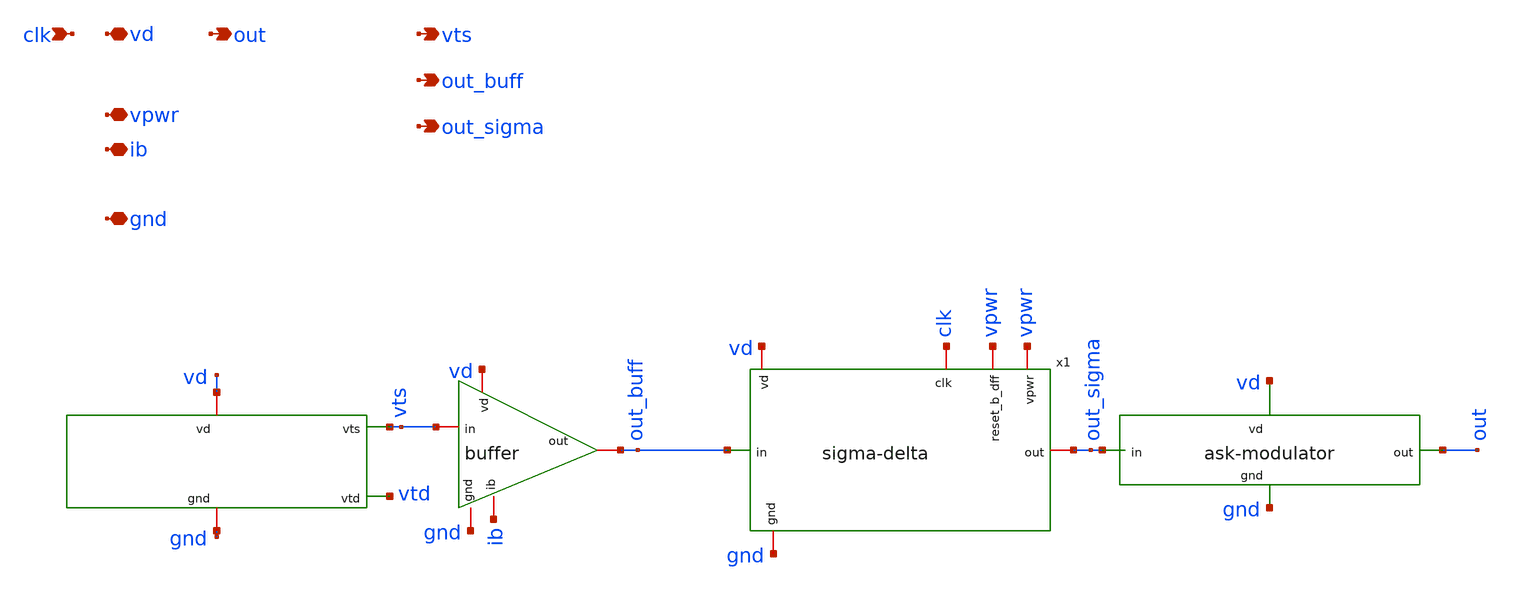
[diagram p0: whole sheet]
** sch_path: device-complete/xschem/device-complete.sch
* buffer/xschem/buffer.sch:
* Copyright 2020 Stefan Frederik Schippers
* Licensed under the Apache License, Version 2.0 (the "License");
**.subckt device-complete vd clk out vpwr ib gnd vts out_buff out_sigma
*.iopin vd
*.ipin clk
*.opin out
*.iopin vpwr
*.iopin ib
*.iopin gnd
*.opin vts
*.opin out_buff
*.opin out_sigma
x3 vd vts vtd gnd sensor
X2 vd vts out_buff ib gnd buffer
x4 vd out out_sigma gnd ask-modulator
x1 vpwr clk out_sigma out_buff vpwr gnd vd sigma-delta
**.ends

* expanding   symbol:  /foss/designs/temp-sensor/sensor/xschem/sensor.sym # of pins=4
** sym_path: sensor/xschem/sensor.sym
** sch_path: sensor/xschem/sensor.sch
.subckt sensor vd vts vtd gnd
*.iopin vd
*.opin vts
*.opin vtd
*.iopin gnd
XP1 a a vd vd sky130_fd_pr__pfet_01v8 L=1 W=4 nf=1 ad='int((nf+1)/2) * W/nf * 0.29' as='int((nf+2)/2) * W/nf * 0.29'
+ pd='2*int((nf+1)/2) * (W/nf + 0.29)' ps='2*int((nf+2)/2) * (W/nf + 0.29)' nrd='0.29 / W' nrs='0.29 / W'
+ sa=0 sb=0 sd=0 mult=1 m=1
XP2 c a d d sky130_fd_pr__pfet_01v8 L=1 W=8 nf=1 ad='int((nf+1)/2) * W/nf * 0.29' as='int((nf+2)/2) * W/nf * 0.29'
+ pd='2*int((nf+1)/2) * (W/nf + 0.29)' ps='2*int((nf+2)/2) * (W/nf + 0.29)' nrd='0.29 / W' nrs='0.29 / W'
+ sa=0 sb=0 sd=0 mult=1 m=1
XP3 d vtd vd vd sky130_fd_pr__pfet_01v8 L=1 W=2 nf=1 ad='int((nf+1)/2) * W/nf * 0.29' as='int((nf+2)/2) * W/nf * 0.29'
+ pd='2*int((nf+1)/2) * (W/nf + 0.29)' ps='2*int((nf+2)/2) * (W/nf + 0.29)' nrd='0.29 / W' nrs='0.29 / W'
+ sa=0 sb=0 sd=0 mult=1 m=1
XP4 vts vtd vd vd sky130_fd_pr__pfet_01v8 L=5 W=2 nf=1 ad='int((nf+1)/2) * W/nf * 0.29' as='int((nf+2)/2) * W/nf * 0.29'
+ pd='2*int((nf+1)/2) * (W/nf + 0.29)' ps='2*int((nf+2)/2) * (W/nf + 0.29)' nrd='0.29 / W' nrs='0.29 / W'
+ sa=0 sb=0 sd=0 mult=1 m=1
XP5 b vtd c c sky130_fd_pr__pfet_01v8 L=1 W=8 nf=1 ad='int((nf+1)/2) * W/nf * 0.29' as='int((nf+2)/2) * W/nf * 0.29'
+ pd='2*int((nf+1)/2) * (W/nf + 0.29)' ps='2*int((nf+2)/2) * (W/nf + 0.29)' nrd='0.29 / W' nrs='0.29 / W'
+ sa=0 sb=0 sd=0 mult=1 m=1
XP6 vtd vtd vts vts sky130_fd_pr__pfet_01v8 L=1 W=16 nf=1 ad='int((nf+1)/2) * W/nf * 0.29' as='int((nf+2)/2) * W/nf * 0.29'
+ pd='2*int((nf+1)/2) * (W/nf + 0.29)' ps='2*int((nf+2)/2) * (W/nf + 0.29)' nrd='0.29 / W' nrs='0.29 / W'
+ sa=0 sb=0 sd=0 mult=1 m=1
XN1 a b gnd gnd sky130_fd_pr__nfet_01v8 L=1 W=1 nf=1 ad='int((nf+1)/2) * W/nf * 0.29' as='int((nf+2)/2) * W/nf * 0.29'
+ pd='2*int((nf+1)/2) * (W/nf + 0.29)' ps='2*int((nf+2)/2) * (W/nf + 0.29)' nrd='0.29 / W' nrs='0.29 / W'
+ sa=0 sb=0 sd=0 mult=8 m=8
XN2 b b gnd gnd sky130_fd_pr__nfet_01v8 L=1 W=1 nf=1 ad='int((nf+1)/2) * W/nf * 0.29' as='int((nf+2)/2) * W/nf * 0.29'
+ pd='2*int((nf+1)/2) * (W/nf + 0.29)' ps='2*int((nf+2)/2) * (W/nf + 0.29)' nrd='0.29 / W' nrs='0.29 / W'
+ sa=0 sb=0 sd=0 mult=8 m=8
XN3 vtd b gnd gnd sky130_fd_pr__nfet_01v8 L=1 W=1 nf=1 ad='int((nf+1)/2) * W/nf * 0.29' as='int((nf+2)/2) * W/nf * 0.29'
+ pd='2*int((nf+1)/2) * (W/nf + 0.29)' ps='2*int((nf+2)/2) * (W/nf + 0.29)' nrd='0.29 / W' nrs='0.29 / W'
+ sa=0 sb=0 sd=0 mult=8 m=8
**** begin user architecture code


R0 a.t0 a.t2 321.179
R1 a a.t0 112.454
R2 a a.t1 7.904
R3 vd.n20 vd.n19 373.458
R4 vd.n21 vd.n20 253.74
R5 vd.n6 vd.n5 103.601
R6 vd.n8 vd.n7 103.152
R7 vd.n9 vd.n8 1.97
R8 vd vd.n22 0.249
R9 vd.n12 vd.n9 0.103
R10 vd.n22 vd.n12 0.071
R11 vd.n12 vd.n11 0.026
R12 vd.n22 vd.n21 0.017
R13 vd.n5 vd.n4 0.015
R14 vd.n19 vd.n18 0.008
R15 vd.n1 vd.n0 0.008
R16 vd.n2 vd.n1 0.007
R17 vd.n20 vd.n17 0.004
R18 vd.n14 vd.n13 0.004
R19 vd.n17 vd.n16 0.003
R20 vd.n15 vd.n14 0.003
R21 vd.n3 vd.n2 0.002
R22 vd.n16 vd.n15 0.002
R23 vd.n9 vd.n6 0.001
R24 vd.n11 vd.n10 0.001
R25 vd.n6 vd.n3 0.001
R26 b.n20 b.t16 37.894
R27 b.n1 b.t14 37.893
R28 b.n7 b.t24 37.891
R29 b.n23 b.t23 37.37
R30 b.n24 b.t18 37.37
R31 b.n25 b.t22 37.37
R32 b.n21 b.t21 37.37
R33 b.n5 b.t10 37.37
R34 b.n12 b.t30 37.37
R35 b.n11 b.t26 37.37
R36 b.n10 b.t31 37.37
R37 b.n8 b.t29 37.37
R38 b.n2 b.t4 37.369
R39 b.n4 b.t0 37.369
R40 b.n6 b.t2 37.369
R41 b.n20 b.t20 37.369
R42 b.n22 b.t17 37.369
R43 b.n1 b.t6 37.369
R44 b.n3 b.t12 37.369
R45 b.n9 b.t25 37.369
R46 b.n7 b.t28 37.369
R47 b.n13 b.t27 37.366
R48 b.n26 b.t19 37.362
R49 b.n0 b.t8 37.358
R50 b.n14 b.t15 17.797
R51 b.n14 b.t7 17.404
R52 b.n15 b.t5 17.404
R53 b.n16 b.t13 17.404
R54 b.n17 b.t1 17.404
R55 b.n18 b.t11 17.404
R56 b.n19 b.t3 17.404
R57 b.n0 b.n13 0.601
R58 b.n26 b.n25 0.555
R59 b.n22 b.n21 0.549
R60 b.n0 b.n6 0.549
R61 b.n13 b.n12 0.548
R62 b.n3 b.n2 0.548
R63 b.n9 b.n8 0.545
R64 b.n25 b.n24 0.524
R65 b.n6 b.n5 0.524
R66 b.n24 b.n23 0.524
R67 b.n5 b.n4 0.524
R68 b.n12 b.n11 0.522
R69 b.n11 b.n10 0.52
R70 b.n4 b.n3 0.492
R71 b.n10 b.n9 0.489
R72 b.n21 b.n20 0.488
R73 b.n2 b.n1 0.488
R74 b.n8 b.n7 0.485
R75 b.t9 b.n19 0.393
R76 b.n19 b.n18 0.393
R77 b.n18 b.n17 0.393
R78 b.n17 b.n16 0.393
R79 b.n16 b.n15 0.393
R80 b.n15 b.n14 0.393
R81 b.n23 b.n22 0.369
R82 b b.n26 0.302
R83 b b.t9 0.237
R84 b b.n0 0.199
R85 gnd.n2 gnd.n10 732.611
R86 gnd.n2 gnd.n8 732.611
R87 gnd.n1 gnd.n14 732.611
R88 gnd.n1 gnd.n12 732.611
R89 gnd.n0 gnd.n6 732.611
R90 gnd.n0 gnd.n4 732.611
R91 gnd.n15 gnd.n2 0.343
R92 gnd gnd.n0 0.285
R93 gnd gnd.n15 0.057
R94 gnd.n15 gnd.n1 0.055
R95 gnd.n10 gnd.n9 0.004
R96 gnd.n8 gnd.n7 0.004
R97 gnd.n14 gnd.n13 0.004
R98 gnd.n12 gnd.n11 0.004
R99 gnd.n6 gnd.n5 0.004
R100 gnd.n4 gnd.n3 0.004
R101 vtd.n0 vtd.t0 401.028
R102 vtd.n2 vtd.t4 209.353
R103 vtd.n2 vtd.t2 65.726
R104 vtd.n1 vtd.t3 13.102
R105 vtd.n0 vtd.t1 5.994
R106 vtd.n1 vtd.n0 0.883
R107 vtd vtd.n3 0.131
R108 vtd.n3 vtd.n2 0.071
R109 vtd.n3 vtd.n1 0.017
R110 vts.n8 vts.n7 107.805
R111 vts.n2 vts.n1 103.152
R112 vts.n9 vts.n8 3.862
R113 vts.n9 vts.n2 0.334
R114 vts vts.n9 0.276
R115 vts.n1 vts.n0 0.015
R116 vts.n5 vts.n4 0.001
R117 vts.n4 vts.n3 0.001
R118 vts.n6 vts.n5 0.001
R119 vts.n8 vts.n6 0.001
C0 vts vtd 0.81fF
C1 c d 1.23fF
C2 b d 0.30fF
C3 vd vts 0.51fF
C4 vtd d 1.98fF
C5 vd d 0.34fF
C6 d a 0.35fF
C7 b c 0.26fF
C8 vtd c 0.44fF
C9 b vtd 1.95fF
C10 vd c 0.07fF
C11 c a 0.53fF
C12 vd b 0.22fF
C13 b a 2.09fF
C14 vd vtd -0.79fF
C15 vtd a 0.62fF
C16 vd a 0.77fF
C17 vts.n0 gnd 2.19fF $ **FLOATING
C18 vts.n1 gnd 0.14fF $ **FLOATING
C19 vts.n2 gnd 0.14fF $ **FLOATING
C20 vts.n3 gnd 0.24fF $ **FLOATING
C21 vts.n4 gnd 0.24fF $ **FLOATING
C22 vts.n6 gnd 4.12fF $ **FLOATING
C23 vts.n7 gnd 2.34fF $ **FLOATING
C24 vts.n8 gnd 0.51fF $ **FLOATING
C25 vts.n9 gnd 2.50fF $ **FLOATING
C26 vtd.t1 gnd 1.23fF
C27 vtd.t0 gnd 2.16fF
C28 vtd.n0 gnd 1.90fF $ **FLOATING
C29 vtd.t3 gnd 2.26fF
C30 vtd.n1 gnd 10.13fF $ **FLOATING
C31 vtd.t4 gnd 1.19fF
C32 vtd.t2 gnd 0.46fF
C33 vtd.n2 gnd 6.89fF $ **FLOATING
C34 vtd.n3 gnd 0.17fF $ **FLOATING
C35 b.n0 gnd 3.50fF $ **FLOATING
C36 b.t14 gnd 2.26fF
C37 b.t6 gnd 2.22fF
C38 b.n1 gnd 5.00fF $ **FLOATING
C39 b.t4 gnd 2.22fF
C40 b.n2 gnd 2.80fF $ **FLOATING
C41 b.t12 gnd 2.22fF
C42 b.n3 gnd 2.76fF $ **FLOATING
C43 b.t0 gnd 2.22fF
C44 b.n4 gnd 2.78fF $ **FLOATING
C45 b.t10 gnd 2.22fF
C46 b.n5 gnd 2.75fF $ **FLOATING
C47 b.t2 gnd 2.22fF
C48 b.n6 gnd 2.85fF $ **FLOATING
C49 b.t24 gnd 2.25fF
C50 b.t28 gnd 2.22fF
C51 b.n7 gnd 4.96fF $ **FLOATING
C52 b.t29 gnd 2.22fF
C53 b.n8 gnd 2.76fF $ **FLOATING
C54 b.t25 gnd 2.22fF
C55 b.n9 gnd 2.77fF $ **FLOATING
C56 b.t31 gnd 2.22fF
C57 b.n10 gnd 2.72fF $ **FLOATING
C58 b.t26 gnd 2.22fF
C59 b.n11 gnd 2.70fF $ **FLOATING
C60 b.t30 gnd 2.22fF
C61 b.n12 gnd 2.79fF $ **FLOATING
C62 b.t27 gnd 2.22fF
C63 b.n13 gnd 3.49fF $ **FLOATING
C64 b.t8 gnd 2.22fF
C65 b.t3 gnd 0.09fF
C66 b.t11 gnd 0.09fF
C67 b.t1 gnd 0.09fF
C68 b.t13 gnd 0.09fF
C69 b.t5 gnd 0.09fF
C70 b.t7 gnd 0.09fF
C71 b.t15 gnd 0.14fF
C72 b.n14 gnd 4.15fF $ **FLOATING
C73 b.n15 gnd 2.33fF $ **FLOATING
C74 b.n16 gnd 2.33fF $ **FLOATING
C75 b.n17 gnd 2.33fF $ **FLOATING
C76 b.n18 gnd 2.33fF $ **FLOATING
C77 b.n19 gnd 2.33fF $ **FLOATING
C78 b.t9 gnd 1.87fF
C79 b.t19 gnd 2.22fF
C80 b.t17 gnd 2.22fF
C81 b.t16 gnd 2.25fF
C82 b.t20 gnd 2.22fF
C83 b.n20 gnd 4.94fF $ **FLOATING
C84 b.t21 gnd 2.22fF
C85 b.n21 gnd 2.75fF $ **FLOATING
C86 b.n22 gnd 11.68fF $ **FLOATING
C87 b.t23 gnd 2.22fF
C88 b.n23 gnd 2.74fF $ **FLOATING
C89 b.t18 gnd 2.22fF
C90 b.n24 gnd 2.75fF $ **FLOATING
C91 b.t22 gnd 2.22fF
C92 b.n25 gnd 2.80fF $ **FLOATING
C93 b.n26 gnd 2.79fF $ **FLOATING
C94 vd.n0 gnd 0.13fF $ **FLOATING
C95 vd.n1 gnd 0.13fF $ **FLOATING
C96 vd.n3 gnd 1.57fF $ **FLOATING
C97 vd.n4 gnd 1.01fF $ **FLOATING
C98 vd.n5 gnd 0.10fF $ **FLOATING
C99 vd.n6 gnd 0.10fF $ **FLOATING
C100 vd.n7 gnd 1.11fF $ **FLOATING
C101 vd.n8 gnd 0.11fF $ **FLOATING
C102 vd.n9 gnd 0.98fF $ **FLOATING
C103 vd.n10 gnd 2.27fF $ **FLOATING
C104 vd.n11 gnd 0.80fF $ **FLOATING
C105 vd.n12 gnd 0.56fF $ **FLOATING
C106 vd.n13 gnd 0.18fF $ **FLOATING
C107 vd.n14 gnd 0.22fF $ **FLOATING
C108 vd.n15 gnd 1.70fF $ **FLOATING
C109 vd.n16 gnd 1.70fF $ **FLOATING
C110 vd.n17 gnd 0.22fF $ **FLOATING
C111 vd.n18 gnd 2.20fF $ **FLOATING
C112 vd.n19 gnd 0.22fF $ **FLOATING
C113 vd.n20 gnd 0.18fF $ **FLOATING
C114 vd.n21 gnd 0.11fF $ **FLOATING
C115 vd.n22 gnd 2.10fF $ **FLOATING
C116 a.t2 gnd 5.67fF
C117 a.t0 gnd 4.55fF
C118 a.t1 gnd 0.28fF
C119 b gnd 147.69fF
C120 vtd gnd 21.99fF
C121 vd gnd 31.07fF
C122 vts gnd 9.31fF
C123 c gnd 15.11fF
C124 d gnd 22.84fF
C125 a gnd 27.99fF


**** end user architecture code
.ends


* expanding   symbol:  /foss/designs/temp-sensor/buffer/xschem/buffer.sym # of pins=5
** sym_path: buffer/xschem/buffer.sym
** sch_path: buffer/xschem/buffer.sch
.subckt buffer vd in out ib gnd
*.iopin vd
*.iopin ib
*.iopin out
*.iopin in
*.iopin gnd
XM3 net2 net2 vd vd sky130_fd_pr__pfet_01v8 L=1 W=1 nf=1 ad='int((nf+1)/2) * W/nf * 0.29' as='int((nf+2)/2) * W/nf * 0.29'
+ pd='2*int((nf+1)/2) * (W/nf + 0.29)' ps='2*int((nf+2)/2) * (W/nf + 0.29)' nrd='0.29 / W' nrs='0.29 / W'
+ sa=0 sb=0 sd=0 mult=1 m=1
XM1 net2 out net4 gnd sky130_fd_pr__nfet_01v8 L=1 W=10 nf=10 ad='int((nf+1)/2) * W/nf * 0.29' as='int((nf+2)/2) * W/nf * 0.29'
+ pd='2*int((nf+1)/2) * (W/nf + 0.29)' ps='2*int((nf+2)/2) * (W/nf + 0.29)' nrd='0.29 / W' nrs='0.29 / W'
+ sa=0 sb=0 sd=0 mult=1 m=1
XM2 net3 in net4 gnd sky130_fd_pr__nfet_01v8 L=1 W=10 nf=10 ad='int((nf+1)/2) * W/nf * 0.29' as='int((nf+2)/2) * W/nf * 0.29'
+ pd='2*int((nf+1)/2) * (W/nf + 0.29)' ps='2*int((nf+2)/2) * (W/nf + 0.29)' nrd='0.29 / W' nrs='0.29 / W'
+ sa=0 sb=0 sd=0 mult=1 m=1
XM4 net3 net3 vd vd sky130_fd_pr__pfet_01v8 L=1 W=1 nf=1 ad='int((nf+1)/2) * W/nf * 0.29' as='int((nf+2)/2) * W/nf * 0.29'
+ pd='2*int((nf+1)/2) * (W/nf + 0.29)' ps='2*int((nf+2)/2) * (W/nf + 0.29)' nrd='0.29 / W' nrs='0.29 / W'
+ sa=0 sb=0 sd=0 mult=1 m=1
XM5 net4 ib gnd gnd sky130_fd_pr__nfet_01v8 L=1 W=1 nf=1 ad='int((nf+1)/2) * W/nf * 0.29' as='int((nf+2)/2) * W/nf * 0.29'
+ pd='2*int((nf+1)/2) * (W/nf + 0.29)' ps='2*int((nf+2)/2) * (W/nf + 0.29)' nrd='0.29 / W' nrs='0.29 / W'
+ sa=0 sb=0 sd=0 mult=1 m=1
XM6 out net3 vd vd sky130_fd_pr__pfet_01v8 L=1 W=10 nf=10 ad='int((nf+1)/2) * W/nf * 0.29' as='int((nf+2)/2) * W/nf * 0.29'
+ pd='2*int((nf+1)/2) * (W/nf + 0.29)' ps='2*int((nf+2)/2) * (W/nf + 0.29)' nrd='0.29 / W' nrs='0.29 / W'
+ sa=0 sb=0 sd=0 mult=1 m=1
XM7 out net1 gnd gnd sky130_fd_pr__nfet_01v8 L=1 W=10 nf=10 ad='int((nf+1)/2) * W/nf * 0.29' as='int((nf+2)/2) * W/nf * 0.29'
+ pd='2*int((nf+1)/2) * (W/nf + 0.29)' ps='2*int((nf+2)/2) * (W/nf + 0.29)' nrd='0.29 / W' nrs='0.29 / W'
+ sa=0 sb=0 sd=0 mult=1 m=1
XM8 net1 net2 vd vd sky130_fd_pr__pfet_01v8 L=1 W=10 nf=10 ad='int((nf+1)/2) * W/nf * 0.29' as='int((nf+2)/2) * W/nf * 0.29'
+ pd='2*int((nf+1)/2) * (W/nf + 0.29)' ps='2*int((nf+2)/2) * (W/nf + 0.29)' nrd='0.29 / W' nrs='0.29 / W'
+ sa=0 sb=0 sd=0 mult=1 m=1
XM9 net1 net1 gnd gnd sky130_fd_pr__nfet_01v8 L=1 W=10 nf=10 ad='int((nf+1)/2) * W/nf * 0.29' as='int((nf+2)/2) * W/nf * 0.29'
+ pd='2*int((nf+1)/2) * (W/nf + 0.29)' ps='2*int((nf+2)/2) * (W/nf + 0.29)' nrd='0.29 / W' nrs='0.29 / W'
+ sa=0 sb=0 sd=0 mult=1 m=1
XM10 ib ib gnd gnd sky130_fd_pr__nfet_01v8 L=1 W=1 nf=1 ad='int((nf+1)/2) * W/nf * 0.29' as='int((nf+2)/2) * W/nf * 0.29'
+ pd='2*int((nf+1)/2) * (W/nf + 0.29)' ps='2*int((nf+2)/2) * (W/nf + 0.29)' nrd='0.29 / W' nrs='0.29 / W'
+ sa=0 sb=0 sd=0 mult=1 m=1
XPD1 net8 net7 net6 net5 sky130_fd_pr__pfet_01v8 L=1 W=1 nf=1 ad='int((nf+1)/2) * W/nf * 0.29' as='int((nf+2)/2) * W/nf * 0.29'
+ pd='2*int((nf+1)/2) * (W/nf + 0.29)' ps='2*int((nf+2)/2) * (W/nf + 0.29)' nrd='0.29 / W' nrs='0.29 / W'
+ sa=0 sb=0 sd=0 mult=1 m=1
XPD2 net12 net11 net10 net9 sky130_fd_pr__pfet_01v8 L=1 W=1 nf=1 ad='int((nf+1)/2) * W/nf * 0.29' as='int((nf+2)/2) * W/nf * 0.29'
+ pd='2*int((nf+1)/2) * (W/nf + 0.29)' ps='2*int((nf+2)/2) * (W/nf + 0.29)' nrd='0.29 / W' nrs='0.29 / W'
+ sa=0 sb=0 sd=0 mult=1 m=1
XPD3 net16 net15 net14 net13 sky130_fd_pr__pfet_01v8 L=1 W=1 nf=1 ad='int((nf+1)/2) * W/nf * 0.29' as='int((nf+2)/2) * W/nf * 0.29'
+ pd='2*int((nf+1)/2) * (W/nf + 0.29)' ps='2*int((nf+2)/2) * (W/nf + 0.29)' nrd='0.29 / W' nrs='0.29 / W'
+ sa=0 sb=0 sd=0 mult=1 m=1
XPD4 net20 net19 net18 net17 sky130_fd_pr__pfet_01v8 L=1 W=1 nf=1 ad='int((nf+1)/2) * W/nf * 0.29' as='int((nf+2)/2) * W/nf * 0.29'
+ pd='2*int((nf+1)/2) * (W/nf + 0.29)' ps='2*int((nf+2)/2) * (W/nf + 0.29)' nrd='0.29 / W' nrs='0.29 / W'
+ sa=0 sb=0 sd=0 mult=1 m=1
XND1 net25 net21 net26 gnd sky130_fd_pr__nfet_01v8 L=1 W=1 nf=1 ad='int((nf+1)/2) * W/nf * 0.29' as='int((nf+2)/2) * W/nf * 0.29'
+ pd='2*int((nf+1)/2) * (W/nf + 0.29)' ps='2*int((nf+2)/2) * (W/nf + 0.29)' nrd='0.29 / W' nrs='0.29 / W'
+ sa=0 sb=0 sd=0 mult=1 m=1
XND2 net27 net22 net28 gnd sky130_fd_pr__nfet_01v8 L=1 W=1 nf=1 ad='int((nf+1)/2) * W/nf * 0.29' as='int((nf+2)/2) * W/nf * 0.29'
+ pd='2*int((nf+1)/2) * (W/nf + 0.29)' ps='2*int((nf+2)/2) * (W/nf + 0.29)' nrd='0.29 / W' nrs='0.29 / W'
+ sa=0 sb=0 sd=0 mult=1 m=1
XND3 net29 net23 net30 gnd sky130_fd_pr__nfet_01v8 L=1 W=1 nf=1 ad='int((nf+1)/2) * W/nf * 0.29' as='int((nf+2)/2) * W/nf * 0.29'
+ pd='2*int((nf+1)/2) * (W/nf + 0.29)' ps='2*int((nf+2)/2) * (W/nf + 0.29)' nrd='0.29 / W' nrs='0.29 / W'
+ sa=0 sb=0 sd=0 mult=1 m=1
XND4 net32 net24 net31 gnd sky130_fd_pr__nfet_01v8 L=1 W=1 nf=1 ad='int((nf+1)/2) * W/nf * 0.29' as='int((nf+2)/2) * W/nf * 0.29'
+ pd='2*int((nf+1)/2) * (W/nf + 0.29)' ps='2*int((nf+2)/2) * (W/nf + 0.29)' nrd='0.29 / W' nrs='0.29 / W'
+ sa=0 sb=0 sd=0 mult=1 m=1
.ends


* expanding   symbol:  /foss/designs/temp-sensor/ask_modulator/xschem/ask-modulator.sym # of pins=4
** sym_path: ask_modulator/xschem/ask-modulator.sym
** sch_path: ask_modulator/xschem/ask-modulator.sch
.subckt ask-modulator vd out in gnd
*.iopin gnd
*.ipin in
*.opin out
*.iopin vd
XC0 vd out sky130_fd_pr__cap_mim_m3_2 W=24.4 L=24.4 MF=3 m=3
XR1 net1 vd gnd sky130_fd_pr__res_xhigh_po_0p35 L=5 mult=1 m=1
XM1 out in gnd gnd sky130_fd_pr__nfet_01v8 L=0.15 W=2 nf=1 ad='int((nf+1)/2) * W/nf * 0.29' as='int((nf+2)/2) * W/nf * 0.29'
+ pd='2*int((nf+1)/2) * (W/nf + 0.29)' ps='2*int((nf+2)/2) * (W/nf + 0.29)' nrd='0.29 / W' nrs='0.29 / W'
+ sa=0 sb=0 sd=0 mult=1 m=1
.ends


* expanding   symbol:  /foss/designs/temp-sensor/sigma-delta_modulator/xschem/sigma-delta.sym # of
*+ pins=7
** sym_path: sigma-delta_modulator/xschem/sigma-delta.sym
** sch_path: sigma-delta_modulator/xschem/sigma-delta.sch
.subckt sigma-delta vpwr clk out in reset_b_dff gnd vd
*.ipin in
*.iopin gnd
*.iopin clk
*.iopin out
*.iopin reset_b_dff
*.iopin vpwr
*.iopin vd
XR2 Q in_int gnd sky130_fd_pr__res_xhigh_po_0p35 L=36 mult=1 m=1
XR1 in_int in gnd sky130_fd_pr__res_xhigh_po_0p35 L=36 mult=1 m=1
XN1 out_comp in_comp gnd gnd sky130_fd_pr__nfet_01v8 L=0.15 W=1 nf=1 ad='int((nf+1)/2) * W/nf * 0.29'
+ as='int((nf+2)/2) * W/nf * 0.29' pd='2*int((nf+1)/2) * (W/nf + 0.29)' ps='2*int((nf+2)/2) * (W/nf + 0.29)'
+ nrd='0.29 / W' nrs='0.29 / W' sa=0 sb=0 sd=0 mult=1 m=1
XP1 out_comp in_comp vd vd sky130_fd_pr__pfet_01v8 L=0.15 W=3 nf=1 ad='int((nf+1)/2) * W/nf * 0.29' as='int((nf+2)/2) * W/nf * 0.29'
+ pd='2*int((nf+1)/2) * (W/nf + 0.29)' ps='2*int((nf+2)/2) * (W/nf + 0.29)' nrd='0.29 / W' nrs='0.29 / W'
+ sa=0 sb=0 sd=0 mult=1 m=1
x1 clk out_comp reset_b_dff GND GND VPWR VPWR Q out sky130_fd_sc_hd__dfrbp_1
XR3 in_comp in_int gnd sky130_fd_pr__res_xhigh_po_0p35 L=18 mult=1 m=1
XC1 in_int gnd sky130_fd_pr__cap_mim_m3_2 W=27.196 L=27.196 MF=1 m=1
XC2 in_comp gnd sky130_fd_pr__cap_mim_m3_2 W=27.196 L=27.196 MF=1 m=1
**** begin user architecture code

.include /foss/pdks/sky130A/libs.ref/sky130_fd_sc_hd/spice/sky130_fd_sc_hd.spice


**** end user architecture code
.ends

.end
